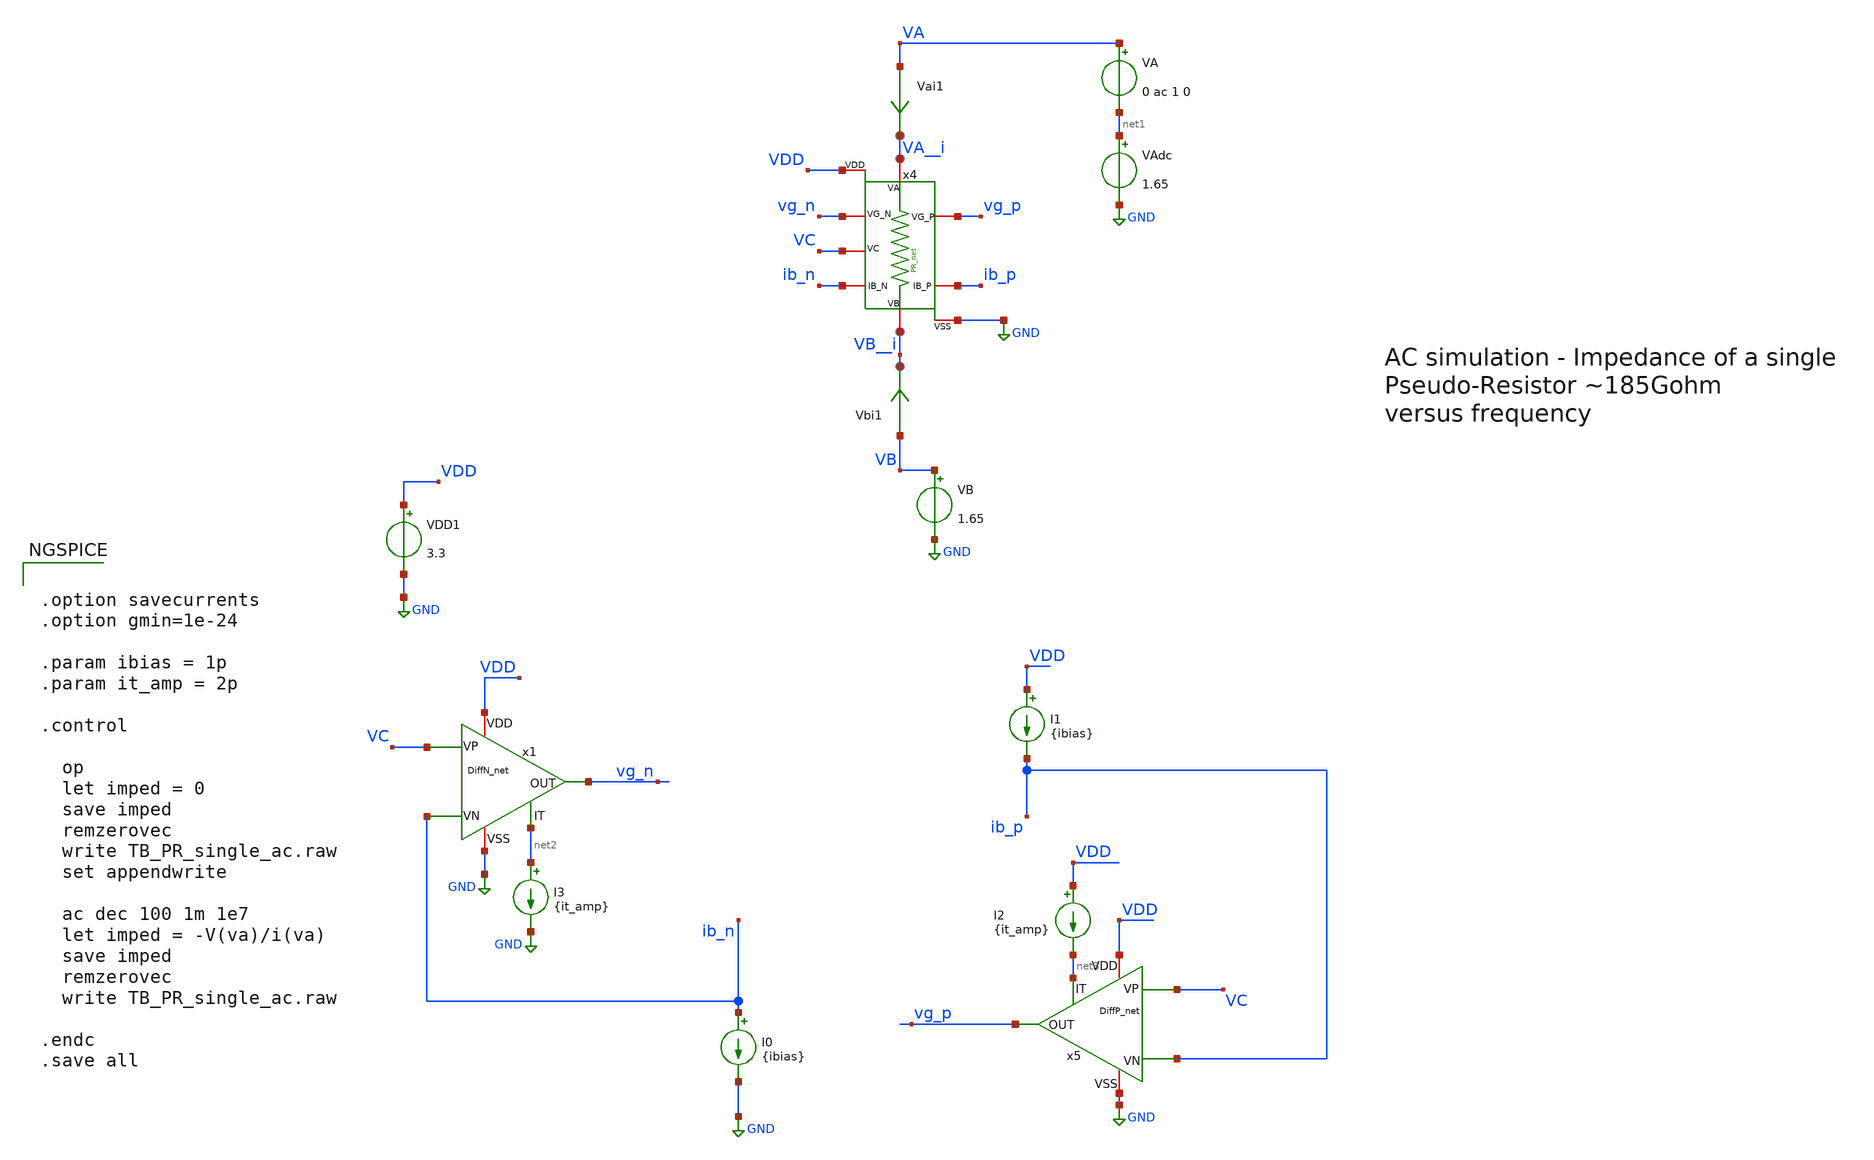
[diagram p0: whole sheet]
** sch_path: TIA/PseudoResistor/TB_PR_single_ac.sch
**.subckt TB_PR_single_ac
VDD1 VDD GND 3.3
VA VA net1 0 ac 1 0
VB VB GND 1.65
VAdc net1 GND 1.65
Vai1 VA VA__i 0
.save i(vai1)
Vbi1 VB VB__i 0
.save i(vbi1)
I0 ib_n GND {ibias}
I1 VDD ib_p {ibias}
I2 VDD net3 {it_amp}
I3 net2 GND {it_amp}
x4 VA__i VB__i vg_n vg_p ib_n ib_p VC VDD GND PR_net
x1 ib_n VC vg_n net2 VDD GND DiffN_net
x5 ib_p VC vg_p net3 VDD GND DiffP_net
**** begin user architecture code


.option savecurrents
.option gmin=1e-24

.param ibias = 1p
.param it_amp = 2p

.control

  op
  let imped = 0
  save imped
  remzerovec
  write TB_PR_single_ac.raw
  set appendwrite

  ac dec 100 1m 1e7
  let imped = -V(va)/i(va)
  save imped
  remzerovec
  write TB_PR_single_ac.raw

.endc
.save all



.include $::180MCU_MODELS/design.ngspice
.lib $::180MCU_MODELS/sm141064.ngspice typical

*.include /home/gmaranhao/Desktop/gf180_work/TIA/PseudoResistor/layout/spice/PR_net_pex.spice

*.subckt PR_net VDD VSS VB VC VA VG_N IB_N IB_P VG_P
*X1 VDD 0 VB__i VC VA__i vg_n ib_n ib_p vg_p PR_net


**** end user architecture code
**.ends
.GLOBAL GND
.end
